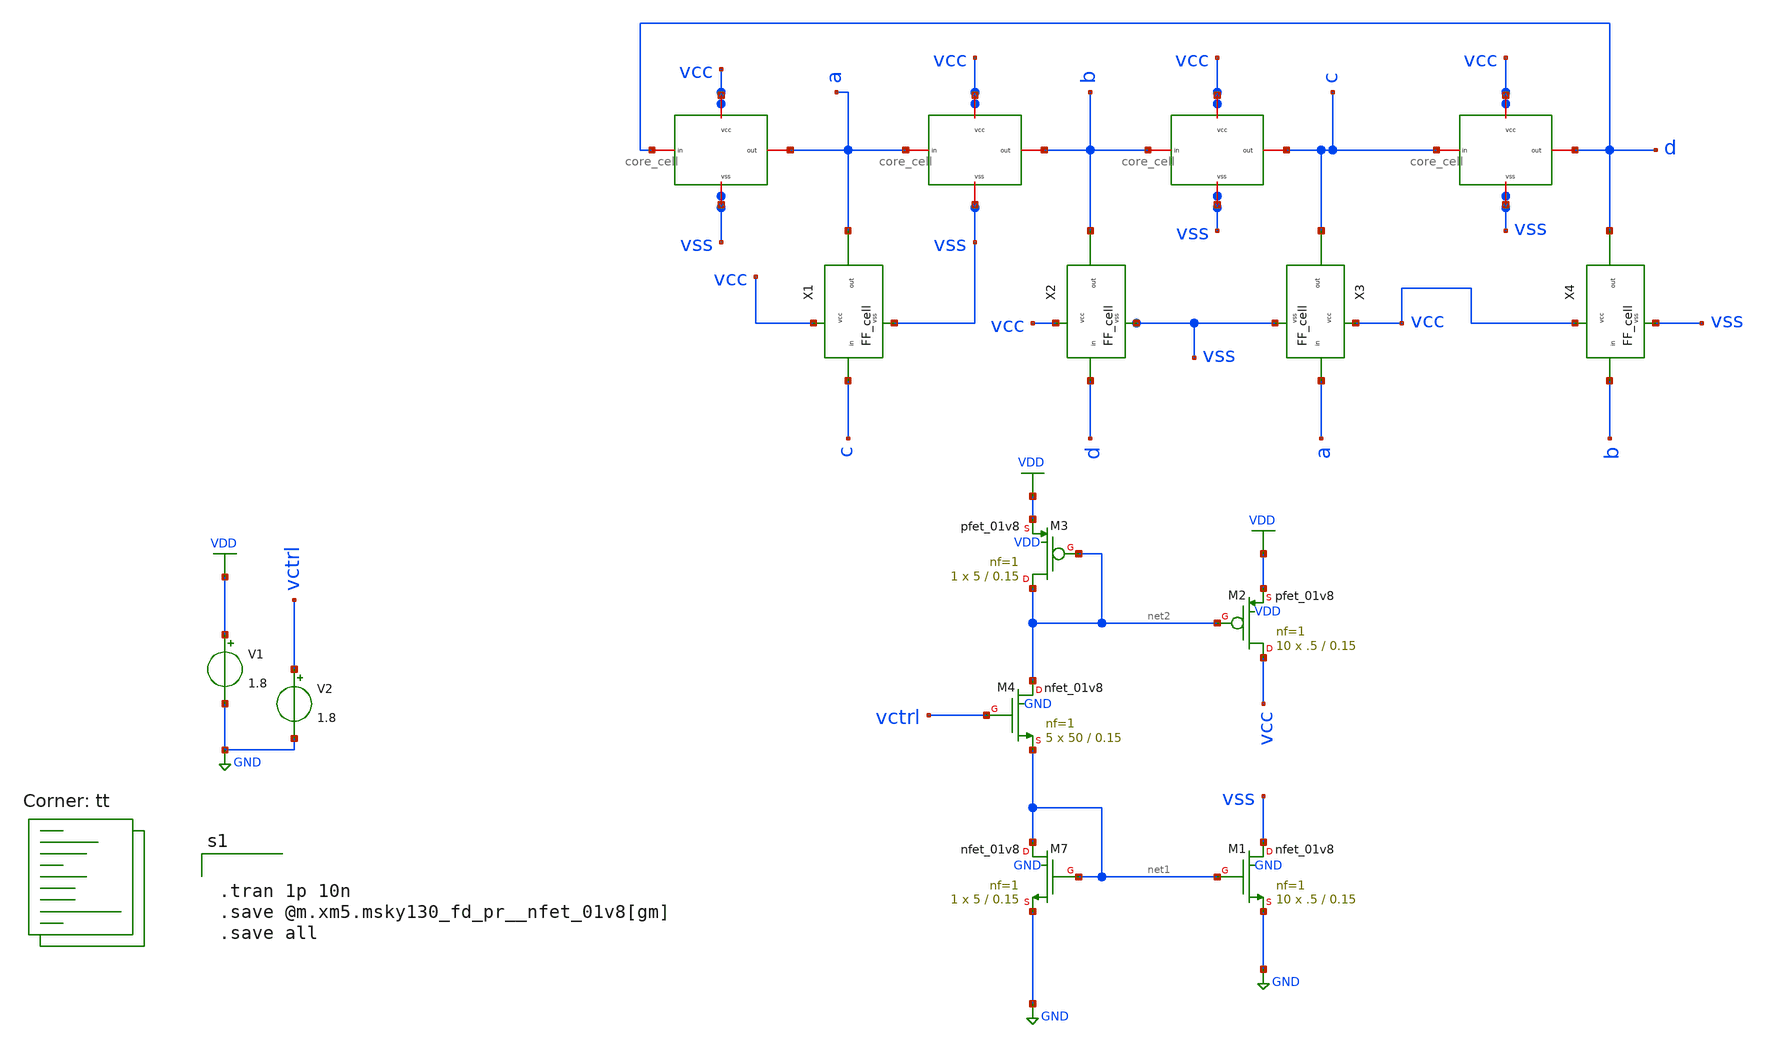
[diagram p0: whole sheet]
** sch_path: pll/ring_vco_lib/QRO_TB/xschem/QRO.sch
**.subckt QRO
V1 VDD GND 1.8
XM1 vss net1 GND GND sky130_fd_pr__nfet_01v8 L=0.15 W=.5 nf=1 ad='int((nf+1)/2) * W/nf * 0.29' as='int((nf+2)/2) * W/nf * 0.29'
+ pd='2*int((nf+1)/2) * (W/nf + 0.29)' ps='2*int((nf+2)/2) * (W/nf + 0.29)' nrd='0.29 / W' nrs='0.29 / W'
+ sa=0 sb=0 sd=0 mult=10 m=10
XM2 vcc net2 VDD VDD sky130_fd_pr__pfet_01v8 L=0.15 W=.5 nf=1 ad='int((nf+1)/2) * W/nf * 0.29' as='int((nf+2)/2) * W/nf * 0.29'
+ pd='2*int((nf+1)/2) * (W/nf + 0.29)' ps='2*int((nf+2)/2) * (W/nf + 0.29)' nrd='0.29 / W' nrs='0.29 / W'
+ sa=0 sb=0 sd=0 mult=10 m=10
V2 vctrl GND 1.8
X1 a vcc vss c FF_cell
X2 b vcc vss d FF_cell
X3 c vcc vss a FF_cell
X4 d vcc vss b FF_cell
X5 vcc a d vss core_cell
X6 vcc b a vss core_cell
X7 vcc c b vss core_cell
X8 vcc d c vss core_cell
XM3 net2 net2 VDD VDD sky130_fd_pr__pfet_01v8 L=0.15 W=5 nf=1 ad='int((nf+1)/2) * W/nf * 0.29' as='int((nf+2)/2) * W/nf * 0.29'
+ pd='2*int((nf+1)/2) * (W/nf + 0.29)' ps='2*int((nf+2)/2) * (W/nf + 0.29)' nrd='0.29 / W' nrs='0.29 / W'
+ sa=0 sb=0 sd=0 mult=1 m=1
XM7 net1 net1 GND GND sky130_fd_pr__nfet_01v8 L=0.15 W=5 nf=1 ad='int((nf+1)/2) * W/nf * 0.29' as='int((nf+2)/2) * W/nf * 0.29'
+ pd='2*int((nf+1)/2) * (W/nf + 0.29)' ps='2*int((nf+2)/2) * (W/nf + 0.29)' nrd='0.29 / W' nrs='0.29 / W'
+ sa=0 sb=0 sd=0 mult=1 m=1
XM4 net2 vctrl net1 GND sky130_fd_pr__nfet_01v8 L=0.15 W=50 nf=1 ad='int((nf+1)/2) * W/nf * 0.29' as='int((nf+2)/2) * W/nf * 0.29'
+ pd='2*int((nf+1)/2) * (W/nf + 0.29)' ps='2*int((nf+2)/2) * (W/nf + 0.29)' nrd='0.29 / W' nrs='0.29 / W'
+ sa=0 sb=0 sd=0 mult=5 m=5
**** begin user architecture code


.tran 1p 10n
.save @m.xm5.msky130_fd_pr__nfet_01v8[gm]
.save all

.lib $::SKYWATER_MODELS/sky130.lib.spice tt
**** end user architecture code
**.ends

* expanding   symbol:  FF_cell.sym # of pins=4
** sym_path: pll/ring_vco_lib/QRO_cell/xschem/FF_cell.sym
** sch_path: pll/ring_vco_lib/QRO_cell/xschem/FF_cell.sch
.subckt FF_cell out vcc vss in
*.ipin vss
*.ipin vcc
*.iopin out
*.iopin in
XM1 out in vss GND sky130_fd_pr__nfet_01v8 L=0.15 W=.5 nf=1 ad='int((nf+1)/2) * W/nf * 0.29' as='int((nf+2)/2) * W/nf * 0.29'
+ pd='2*int((nf+1)/2) * (W/nf + 0.29)' ps='2*int((nf+2)/2) * (W/nf + 0.29)' nrd='0.29 / W' nrs='0.29 / W'
+ sa=0 sb=0 sd=0 mult=1 m=1
XM2 out in vcc VDD sky130_fd_pr__pfet_01v8 L=0.15 W=1 nf=1 ad='int((nf+1)/2) * W/nf * 0.29' as='int((nf+2)/2) * W/nf * 0.29'
+ pd='2*int((nf+1)/2) * (W/nf + 0.29)' ps='2*int((nf+2)/2) * (W/nf + 0.29)' nrd='0.29 / W' nrs='0.29 / W'
+ sa=0 sb=0 sd=0 mult=1 m=1
.ends


* expanding   symbol:  core_cell.sym # of pins=4
** sym_path: pll/ring_vco_lib/QRO_cell/xschem/core_cell.sym
** sch_path: pll/ring_vco_lib/QRO_cell/xschem/core_cell.sch
.subckt core_cell vcc out in vss
*.ipin vcc
*.ipin vss
*.iopin in
*.iopin out
XM1 out in vss GND sky130_fd_pr__nfet_01v8 L=0.15 W=1 nf=1 ad='int((nf+1)/2) * W/nf * 0.29' as='int((nf+2)/2) * W/nf * 0.29'
+ pd='2*int((nf+1)/2) * (W/nf + 0.29)' ps='2*int((nf+2)/2) * (W/nf + 0.29)' nrd='0.29 / W' nrs='0.29 / W'
+ sa=0 sb=0 sd=0 mult=1 m=1
XM2 out in vcc VDD sky130_fd_pr__pfet_01v8 L=0.15 W=2 nf=1 ad='int((nf+1)/2) * W/nf * 0.29' as='int((nf+2)/2) * W/nf * 0.29'
+ pd='2*int((nf+1)/2) * (W/nf + 0.29)' ps='2*int((nf+2)/2) * (W/nf + 0.29)' nrd='0.29 / W' nrs='0.29 / W'
+ sa=0 sb=0 sd=0 mult=1 m=1
.ends

.GLOBAL VDD
.GLOBAL GND
.end
